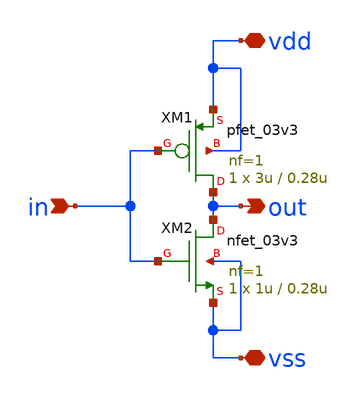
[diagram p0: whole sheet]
** sch_path: xschem/symbols/gf180mcu_03v3_inv1.sch
* Copyright 2021 Stefan Frederik Schippers
* Licensed under the Apache License, Version 2.0 (the "License");
* you may not use this file except in compliance with the License.
* You may obtain a copy of the License at
* https://www.apache.org/licenses/LICENSE-2.0
* Unless required by applicable law or agreed to in writing, software
* distributed under the License is distributed on an "AS IS" BASIS,
* WITHOUT WARRANTIES OR CONDITIONS OF ANY KIND, either express or implied.
* See the License for the specific language governing permissions and
* limitations under the License.
**.subckt gf180mcu_03v3_inv1 vdd vss in out
*.iopin vdd
*.iopin vss
*.ipin in
*.opin out
XM1 out in vdd vdd pfet_03v3 L=0.28u W=3u nf=1 ad='int((nf+1)/2) * W/nf * 0.18u' as='int((nf+2)/2) * W/nf * 0.18u'
+ pd='2*int((nf+1)/2) * (W/nf + 0.18u)' ps='2*int((nf+2)/2) * (W/nf + 0.18u)' nrd='0.18u / W' nrs='0.18u / W'
+ sa=0 sb=0 sd=0 m=1
XM2 out in vss vss nfet_03v3 L=0.28u W=1u nf=1 ad='int((nf+1)/2) * W/nf * 0.18u' as='int((nf+2)/2) * W/nf * 0.18u'
+ pd='2*int((nf+1)/2) * (W/nf + 0.18u)' ps='2*int((nf+2)/2) * (W/nf + 0.18u)' nrd='0.18u / W' nrs='0.18u / W'
+ sa=0 sb=0 sd=0 m=1
**.ends
.end
